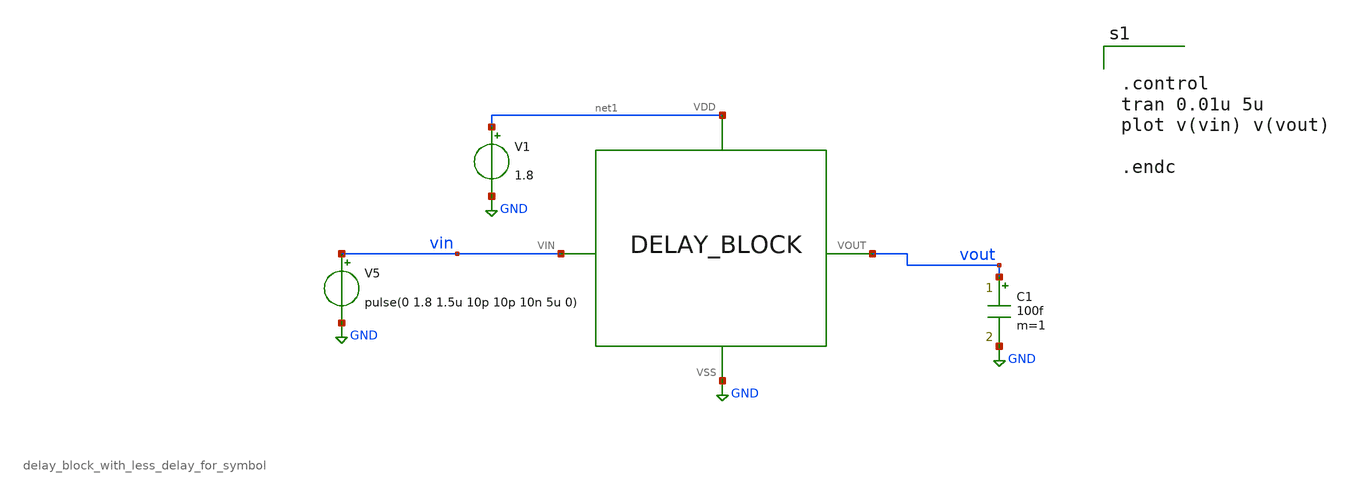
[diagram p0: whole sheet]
** sch_path: xschem/DC_DC_Converter_xschem/OTHERS/DC_DC_Converter_JV10/Delay_block_revised/delay_bpock_tb.sch
**.subckt delay_bpock_tb
V1 net1 GND 1.8
V5 vin GND pulse(0 1.8 1.5u 10p 10p 10n 5u 0)
C1 vout GND 100f m=1
X1 vin vout net1 GND delay_block_with_less_delay_for_symbol
**** begin user architecture code


.control
tran 0.01u 5u
plot v(vin) v(vout)

.endc



** opencircuitdesign pdks install
.lib $::SKYWATER_MODELS/sky130.lib.spice tt


**** end user architecture code
**.ends
.GLOBAL GND
.end
